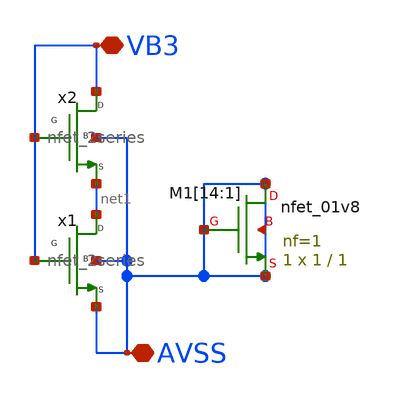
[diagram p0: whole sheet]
** sch_path: INA_layout_v2/bias/nbias_vb3.sch
**.subckt nbias_vb3 AVSS VB3
*.iopin AVSS
*.iopin VB3
x1 AVSS AVSS VB3 net1 nfet_2series
x2 net1 AVSS VB3 VB3 nfet_2series
XM1[14] AVSS AVSS AVSS AVSS sky130_fd_pr__nfet_01v8 L=1 W=1 nf=1 ad='int((nf+1)/2) * W/nf * 0.29' as='int((nf+2)/2) * W/nf * 0.29'
+ pd='2*int((nf+1)/2) * (W/nf + 0.29)' ps='2*int((nf+2)/2) * (W/nf + 0.29)' nrd='0.29 / W' nrs='0.29 / W'
+ sa=0 sb=0 sd=0 mult=1 m=1
XM1[13] AVSS AVSS AVSS AVSS sky130_fd_pr__nfet_01v8 L=1 W=1 nf=1 ad='int((nf+1)/2) * W/nf * 0.29' as='int((nf+2)/2) * W/nf * 0.29'
+ pd='2*int((nf+1)/2) * (W/nf + 0.29)' ps='2*int((nf+2)/2) * (W/nf + 0.29)' nrd='0.29 / W' nrs='0.29 / W'
+ sa=0 sb=0 sd=0 mult=1 m=1
XM1[12] AVSS AVSS AVSS AVSS sky130_fd_pr__nfet_01v8 L=1 W=1 nf=1 ad='int((nf+1)/2) * W/nf * 0.29' as='int((nf+2)/2) * W/nf * 0.29'
+ pd='2*int((nf+1)/2) * (W/nf + 0.29)' ps='2*int((nf+2)/2) * (W/nf + 0.29)' nrd='0.29 / W' nrs='0.29 / W'
+ sa=0 sb=0 sd=0 mult=1 m=1
XM1[11] AVSS AVSS AVSS AVSS sky130_fd_pr__nfet_01v8 L=1 W=1 nf=1 ad='int((nf+1)/2) * W/nf * 0.29' as='int((nf+2)/2) * W/nf * 0.29'
+ pd='2*int((nf+1)/2) * (W/nf + 0.29)' ps='2*int((nf+2)/2) * (W/nf + 0.29)' nrd='0.29 / W' nrs='0.29 / W'
+ sa=0 sb=0 sd=0 mult=1 m=1
XM1[10] AVSS AVSS AVSS AVSS sky130_fd_pr__nfet_01v8 L=1 W=1 nf=1 ad='int((nf+1)/2) * W/nf * 0.29' as='int((nf+2)/2) * W/nf * 0.29'
+ pd='2*int((nf+1)/2) * (W/nf + 0.29)' ps='2*int((nf+2)/2) * (W/nf + 0.29)' nrd='0.29 / W' nrs='0.29 / W'
+ sa=0 sb=0 sd=0 mult=1 m=1
XM1[9] AVSS AVSS AVSS AVSS sky130_fd_pr__nfet_01v8 L=1 W=1 nf=1 ad='int((nf+1)/2) * W/nf * 0.29' as='int((nf+2)/2) * W/nf * 0.29'
+ pd='2*int((nf+1)/2) * (W/nf + 0.29)' ps='2*int((nf+2)/2) * (W/nf + 0.29)' nrd='0.29 / W' nrs='0.29 / W'
+ sa=0 sb=0 sd=0 mult=1 m=1
XM1[8] AVSS AVSS AVSS AVSS sky130_fd_pr__nfet_01v8 L=1 W=1 nf=1 ad='int((nf+1)/2) * W/nf * 0.29' as='int((nf+2)/2) * W/nf * 0.29'
+ pd='2*int((nf+1)/2) * (W/nf + 0.29)' ps='2*int((nf+2)/2) * (W/nf + 0.29)' nrd='0.29 / W' nrs='0.29 / W'
+ sa=0 sb=0 sd=0 mult=1 m=1
XM1[7] AVSS AVSS AVSS AVSS sky130_fd_pr__nfet_01v8 L=1 W=1 nf=1 ad='int((nf+1)/2) * W/nf * 0.29' as='int((nf+2)/2) * W/nf * 0.29'
+ pd='2*int((nf+1)/2) * (W/nf + 0.29)' ps='2*int((nf+2)/2) * (W/nf + 0.29)' nrd='0.29 / W' nrs='0.29 / W'
+ sa=0 sb=0 sd=0 mult=1 m=1
XM1[6] AVSS AVSS AVSS AVSS sky130_fd_pr__nfet_01v8 L=1 W=1 nf=1 ad='int((nf+1)/2) * W/nf * 0.29' as='int((nf+2)/2) * W/nf * 0.29'
+ pd='2*int((nf+1)/2) * (W/nf + 0.29)' ps='2*int((nf+2)/2) * (W/nf + 0.29)' nrd='0.29 / W' nrs='0.29 / W'
+ sa=0 sb=0 sd=0 mult=1 m=1
XM1[5] AVSS AVSS AVSS AVSS sky130_fd_pr__nfet_01v8 L=1 W=1 nf=1 ad='int((nf+1)/2) * W/nf * 0.29' as='int((nf+2)/2) * W/nf * 0.29'
+ pd='2*int((nf+1)/2) * (W/nf + 0.29)' ps='2*int((nf+2)/2) * (W/nf + 0.29)' nrd='0.29 / W' nrs='0.29 / W'
+ sa=0 sb=0 sd=0 mult=1 m=1
XM1[4] AVSS AVSS AVSS AVSS sky130_fd_pr__nfet_01v8 L=1 W=1 nf=1 ad='int((nf+1)/2) * W/nf * 0.29' as='int((nf+2)/2) * W/nf * 0.29'
+ pd='2*int((nf+1)/2) * (W/nf + 0.29)' ps='2*int((nf+2)/2) * (W/nf + 0.29)' nrd='0.29 / W' nrs='0.29 / W'
+ sa=0 sb=0 sd=0 mult=1 m=1
XM1[3] AVSS AVSS AVSS AVSS sky130_fd_pr__nfet_01v8 L=1 W=1 nf=1 ad='int((nf+1)/2) * W/nf * 0.29' as='int((nf+2)/2) * W/nf * 0.29'
+ pd='2*int((nf+1)/2) * (W/nf + 0.29)' ps='2*int((nf+2)/2) * (W/nf + 0.29)' nrd='0.29 / W' nrs='0.29 / W'
+ sa=0 sb=0 sd=0 mult=1 m=1
XM1[2] AVSS AVSS AVSS AVSS sky130_fd_pr__nfet_01v8 L=1 W=1 nf=1 ad='int((nf+1)/2) * W/nf * 0.29' as='int((nf+2)/2) * W/nf * 0.29'
+ pd='2*int((nf+1)/2) * (W/nf + 0.29)' ps='2*int((nf+2)/2) * (W/nf + 0.29)' nrd='0.29 / W' nrs='0.29 / W'
+ sa=0 sb=0 sd=0 mult=1 m=1
XM1[1] AVSS AVSS AVSS AVSS sky130_fd_pr__nfet_01v8 L=1 W=1 nf=1 ad='int((nf+1)/2) * W/nf * 0.29' as='int((nf+2)/2) * W/nf * 0.29'
+ pd='2*int((nf+1)/2) * (W/nf + 0.29)' ps='2*int((nf+2)/2) * (W/nf + 0.29)' nrd='0.29 / W' nrs='0.29 / W'
+ sa=0 sb=0 sd=0 mult=1 m=1
**.ends

* expanding   symbol:  INA_layout_v2/bias/nfet_2series.sym # of pins=4
** sym_path: INA_layout_v2/bias/nfet_2series.sym
** sch_path: INA_layout_v2/bias/nfet_2series.sch
.subckt nfet_2series S B G D
*.iopin S
*.iopin B
*.iopin G
*.iopin D
XM1 D G net1 B sky130_fd_pr__nfet_01v8 L=1 W=1 nf=1 ad='int((nf+1)/2) * W/nf * 0.29' as='int((nf+2)/2) * W/nf * 0.29'
+ pd='2*int((nf+1)/2) * (W/nf + 0.29)' ps='2*int((nf+2)/2) * (W/nf + 0.29)' nrd='0.29 / W' nrs='0.29 / W'
+ sa=0 sb=0 sd=0 mult=1 m=1
XM2 net1 G S B sky130_fd_pr__nfet_01v8 L=1 W=1 nf=1 ad='int((nf+1)/2) * W/nf * 0.29' as='int((nf+2)/2) * W/nf * 0.29'
+ pd='2*int((nf+1)/2) * (W/nf + 0.29)' ps='2*int((nf+2)/2) * (W/nf + 0.29)' nrd='0.29 / W' nrs='0.29 / W'
+ sa=0 sb=0 sd=0 mult=1 m=1
.ends

.end
